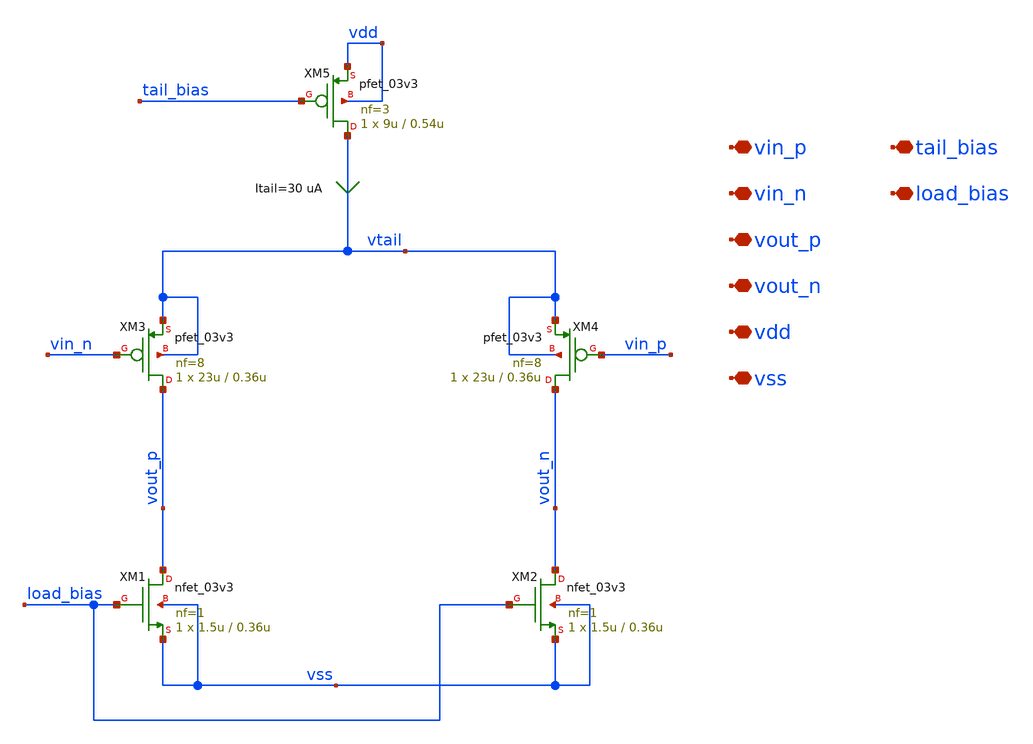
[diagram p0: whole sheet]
** sch_path: xschem/input_stage/input_stage.sch
**.subckt input_stage vin_p vin_n vout_p vout_n vdd vss tail_bias load_bias
*.iopin vin_p
*.iopin vin_n
*.iopin vout_p
*.iopin vout_n
*.iopin vdd
*.iopin vss
*.iopin tail_bias
*.iopin load_bias
XM1 vout_p load_bias vss vss nfet_03v3 L=0.36u W=1.5u nf=1 ad='int((nf+1)/2) * W/nf * 0.18u' as='int((nf+2)/2) * W/nf * 0.18u'
+ pd='2*int((nf+1)/2) * (W/nf + 0.18u)' ps='2*int((nf+2)/2) * (W/nf + 0.18u)' nrd='0.18u / W' nrs='0.18u / W'
+ sa=0 sb=0 sd=0 m=1
XM2 vout_n load_bias vss vss nfet_03v3 L=0.36u W=1.5u nf=1 ad='int((nf+1)/2) * W/nf * 0.18u' as='int((nf+2)/2) * W/nf * 0.18u'
+ pd='2*int((nf+1)/2) * (W/nf + 0.18u)' ps='2*int((nf+2)/2) * (W/nf + 0.18u)' nrd='0.18u / W' nrs='0.18u / W'
+ sa=0 sb=0 sd=0 m=1
XM3 vout_p vin_n vtail vtail pfet_03v3 L=0.36u W=23u nf=8 ad='int((nf+1)/2) * W/nf * 0.18u' as='int((nf+2)/2) * W/nf * 0.18u'
+ pd='2*int((nf+1)/2) * (W/nf + 0.18u)' ps='2*int((nf+2)/2) * (W/nf + 0.18u)' nrd='0.18u / W' nrs='0.18u / W'
+ sa=0 sb=0 sd=0 m=1
XM5 vtail tail_bias vdd vdd pfet_03v3 L=0.54u W=9u nf=3 ad='int((nf+1)/2) * W/nf * 0.18u' as='int((nf+2)/2) * W/nf * 0.18u'
+ pd='2*int((nf+1)/2) * (W/nf + 0.18u)' ps='2*int((nf+2)/2) * (W/nf + 0.18u)' nrd='0.18u / W' nrs='0.18u / W'
+ sa=0 sb=0 sd=0 m=1
XM4 vout_n vin_p vtail vtail pfet_03v3 L=0.36u W=23u nf=8 ad='int((nf+1)/2) * W/nf * 0.18u' as='int((nf+2)/2) * W/nf * 0.18u'
+ pd='2*int((nf+1)/2) * (W/nf + 0.18u)' ps='2*int((nf+2)/2) * (W/nf + 0.18u)' nrd='0.18u / W' nrs='0.18u / W'
+ sa=0 sb=0 sd=0 m=1
**.ends
.end
